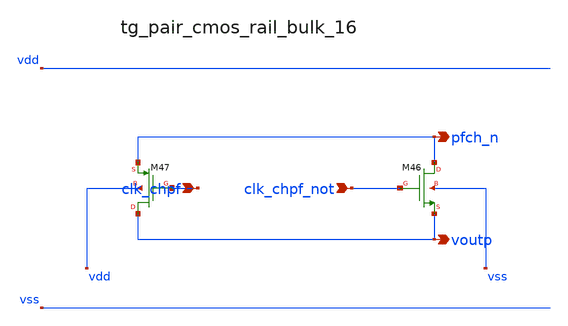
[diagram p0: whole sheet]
** sch_path: analog-db/raw/ia_003_fan_chopper_pf/hier/blocks/tg_pair_cmos_rail_bulk_16.sch
**.subckt tg_pair_cmos_rail_bulk_16 clk_chpf clk_chpf_not pfch_n voutp
*.ipin clk_chpf
*.ipin clk_chpf_not
*.opin pfch_n
*.opin voutp
XM46 pfch_n clk_chpf_not voutp vss sg13_lv_nmos w=x_dut_xm46_w l=x_dut_xm46_l ng=1 m=x_dut_xm46_m
XM47 voutp clk_chpf pfch_n vdd sg13_lv_pmos w=x_dut_xm47_w l=x_dut_xm47_l ng=1 m=x_dut_xm47_m
**.ends
.end
